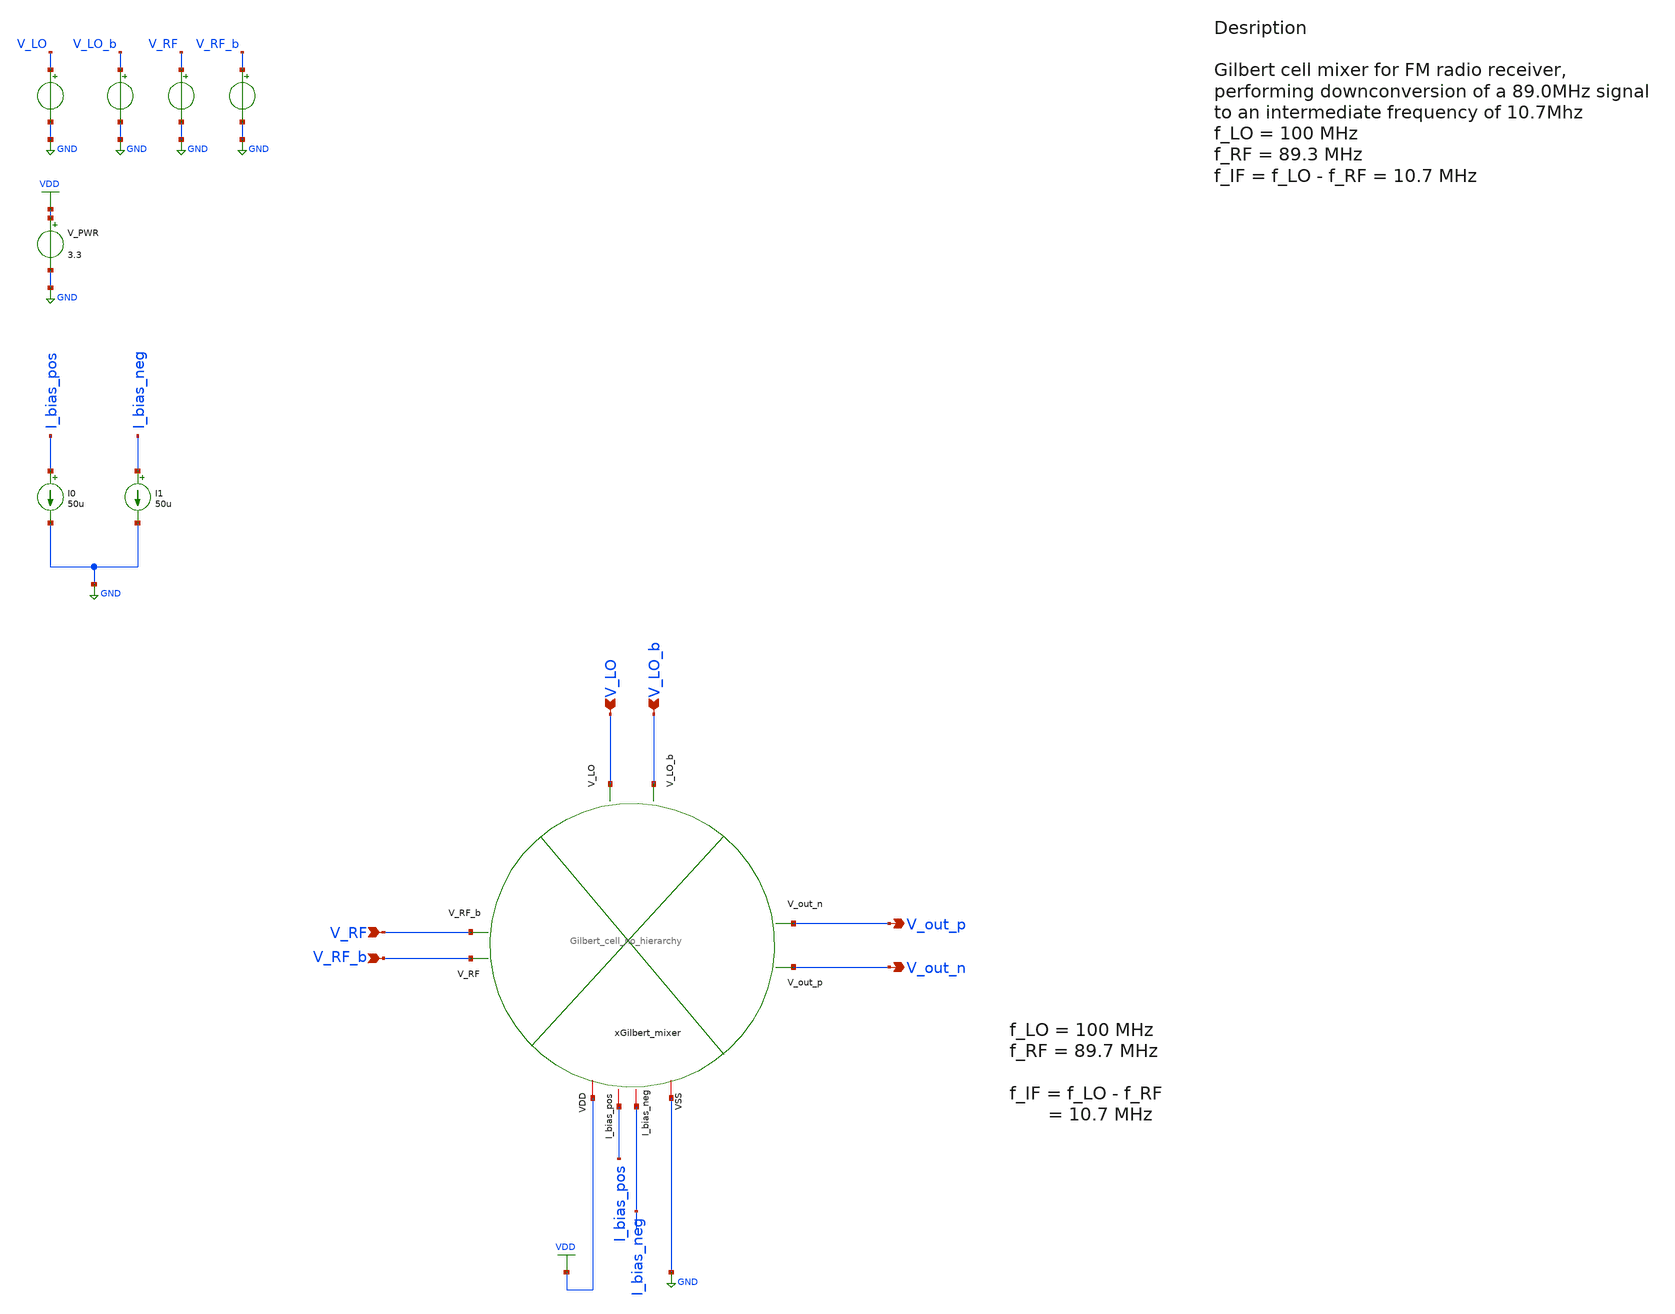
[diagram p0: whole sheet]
** sch_path: src/design_tb/Gilbert_cell_tb.sch
**.subckt Gilbert_cell_tb V_LO V_LO_b V_RF V_RF_b V_out_p V_out_n
*.ipin V_LO
*.ipin V_LO_b
*.ipin V_RF
*.ipin V_RF_b
*.opin V_out_p
*.opin V_out_n
V_PWR VDD GND 3.3
.save i(v_pwr)
V_LO V_LO GND pulse(0 1.5 0 1p 1p 0.25n 0.5n)
.save i(v_lo)
V_LO_b V_LO_b GND pulse(0 1.5 0 1p 1p 0.25n 0.5n)
.save i(v_lo_b)
V_RF V_RF GND sin( 1 1 1 0 )
.save i(v_rf)
V_RF_b V_RF_b GND sin( 1 1 1 0 0 180 )
.save i(v_rf_b)
xGilbert_mixer VDD V_out_n V_out_p V_LO V_LO_b V_RF_b V_RF I_bias_pos I_bias_neg GND
+ Gilbert_cell_no_hierarchy
I0 I_bias_pos GND 50u
I1 I_bias_neg GND 50u
**** begin user architecture code

.include $::180MCU_MODELS/design.ngspice
.lib $::180MCU_MODELS/sm141064.ngspice typical
.lib $::180MCU_MODELS/sm141064.ngspice mimcap_typical
.lib $::180MCU_MODELS/sm141064.ngspice cap_mim
.lib $::180MCU_MODELS/sm141064.ngspice res_typical




* let sets vectors to a plot, while set sets a variable, globally accessible in .control
.control

    * Set frequency and amplitude variables to proper values from within the control sequence
    * sine-wave LO
    * set cm_lo = 0.5
    * set freq_lo = 2.50G
    * set amp_lo = 0.5
    * alter @V_LO[sin] = [ $cm_lo $amp_lo $freq_lo 0 ]
    * alter @V_LO_b[sin] = [ $cm_lo $amp_lo $freq_lo 0 0 180 ]

    set freq_lo = 100Meg
    set cm_lo = 1.8
    set amp_lo = 0.4

    set cm_rf  = 1.2
    set freq_rf = 89.3Meg
    * set freq_rf = 10.7Meg
    set amp_rf  = 0.2

    * set the parameters to the voltage sources
    * alter @V_LO[pulse] = [ 2 2.5 0 0.5p 0.5p 5n 10n ]
    * alter @V_LO_b[pulse] = [ 2 2.5 5n 0.5p 0.5p 5n 10n]
    alter @V_LO[sin] = [ $cm_lo $amp_lo $freq_lo 0 ]
    alter @V_LO_b[sin] = [ $cm_lo $amp_lo $freq_lo 0 0 180 ]
    alter @V_RF[sin] = [ $cm_rf $amp_rf $freq_rf 0 ]
    alter @V_RF_b[sin] = [ $cm_rf $amp_rf $freq_rf 0 0 180 ]

    save all

    * operating point
    op
    show

    * save transistor op parameters
    * diff_pair_1 transistors
    save @m.xgilbert_mixer.xm_rf_pos.m0[vgs]
    save @m.xgilbert_mixer.xm_rf_pos.m0[vds]
    save @m.xgilbert_mixer.xm_rf_pos.m0[id]
    save @m.xgilbert_mixer.xm_rf_pos.m0[gm]
    save @m.xgilbert_mixer.xm_rf_pos.m0[vth]
    save @m.xgilbert_mixer.xm_rf_pos.m0[cgg]
    save @m.xgilbert_mixer.xm_rf_neg.m0[vgs]
    save @m.xgilbert_mixer.xm_rf_neg.m0[vds]
    save @m.xgilbert_mixer.xm_rf_neg.m0[id]
    save @m.xgilbert_mixer.xm_rf_neg.m0[gm]
    save @m.xgilbert_mixer.xm_rf_neg.m0[vth]
    save @m.xgilbert_mixer.xm_rf_neg.m0[cgg]

    * diff_pair_2 transistors
    * save @m.xdiff_pair_2.xm1.m0[vgs]
    * save @m.xdiff_pair_2.xm1.m0[vds]
    * save @m.xdiff_pair_2.xm1.m0[id]
    * save @m.xdiff_pair_2.xm1.m0[gm]
    * save @m.xdiff_pair_2.xm1.m0[vth]
    * save @m.xdiff_pair_2.xm1.m0[cgg]
    * save @m.xdiff_pair_2.xm2.m0[vgs]
    * save @m.xdiff_pair_2.xm2.m0[vds]
    * save @m.xdiff_pair_2.xm2.m0[id]
    * save @m.xdiff_pair_2.xm2.m0[gm]
    * save @m.xdiff_pair_2.xm2.m0[vth]
    * save @m.xdiff_pair_2.xm2.m0[cgg]

    * diff_pair_3 transistors
    * save @m.xdiff_pair_3.xm1.m0[vgs]
    * save @m.xdiff_pair_3.xm1.m0[vds]
    * save @m.xdiff_pair_3.xm1.m0[id]
    * save @m.xdiff_pair_3.xm1.m0[gm]
    * save @m.xdiff_pair_3.xm1.m0[vth]
    * save @m.xdiff_pair_3.xm1.m0[cgg]
    * save @m.xdiff_pair_3.xm2.m0[vgs]
    * save @m.xdiff_pair_3.xm2.m0[vds]
    * save @m.xdiff_pair_3.xm2.m0[id]
    * save @m.xdiff_pair_3.xm2.m0[gm]
    * save @m.xdiff_pair_3.xm2.m0[vth]
    * save @m.xdiff_pair_3.xm2.m0[cgg]

    write Gilbert_cell_tb_sim.raw

    set appendwrite

    * Transient analysis to observe mixing operation
    tran 1p 0.3u
    write Gilbert_cell_tb_sim.raw

    * Calculate differential output for conversion gain measurement
    let v_out_diff = v(v_out_p)-v(v_out_n)
    let v_rf_diff = v(v_rf)-v(v_rf_b)
    let v_lo_diff = v(v_lo)-v(v_lo_b)


    * Extract IF component at 100MHz using FFT
    linearize v_out_diff v_rf_diff v_lo_diff
    let time_step = 1e-12
    let sample_freq = 1/time_step
    let npts = length(v_out_diff)
    let freq_res = sample_freq/npts


    fft v_out_diff v_rf_diff v_lo_diff

    * print everything, sanity check
    * set     ; print all available global (?) variables (?)
    * setplot ; print all plots
    * display ; print variables available in current plot

    let freq_res = tran2.freq_res
    let freq_if = abs ( $freq_lo - $freq_rf )

    * Define bandwidth for power integration (10MHz around nominal frequencies).
    *  To improve resolution increase time of tran simulation, reduce time step, in order to reduce
+ FFT resolution
    let bandwidth = 10e6
    let bin_width = floor(bandwidth/freq_res + 0.5)

    * Find center bins for RF and IF frequencies
    let rf_center_bin = floor( $freq_rf/freq_res + 0.5 )
    let if_center_bin = floor( freq_if/freq_res + 0.5 )

    * Calculate power by summing magnitude squared over the bandwidth
    * RF power integration (±10MHz around freq_rf)
    let rf_power_total = 0
    let i = rf_center_bin - bin_width
    while i <= rf_center_bin + bin_width
        if i>0 & i < length(v_rf_diff)
            let bin_freq = i * freq_res
            * print bin_freq
            * print abs(v_rf_diff[i])
            let rf_power_total = rf_power_total + abs(v_rf_diff[i])^2
        end
        let i = i + 1
    end

    * IF power integration (±10MHz around freq_if)
    let if_power_total = 0
    let j = if_center_bin - bin_width
    while j <= if_center_bin + bin_width
        if j >= 0 & j < length(v_out_diff)
            let bin_freq = j * freq_res
            * print bin_freq
            * print abs(v_out_diff[j])
            let if_power_total = if_power_total + abs(v_out_diff[j])^2
        end
        let j = j + 1
    end

    print if_power_total
    print rf_power_total

    let conversion_gain_db = 10*log10(if_power_total/rf_power_total)
    print conversion_gain_db

    write Gilbert_cell_tb_sim.raw

.endc


**** end user architecture code
**.ends

* expanding   symbol:
*+  /home/vasil/Downloads/SSCS_PICO_2025/src/design_xsch/Gilbert_cell_no_hierarchy.sym # of pins=10
** sym_path: src/design_xsch/experimental_hierarchal/Gilbert_cell_no_hierarchy.sym
** sch_path: src/design_xsch/experimental_hierarchal/Gilbert_cell_no_hierarchy.sch
.subckt Gilbert_cell_no_hierarchy VDD V_out_p V_out_n V_LO V_LO_b V_RF V_RF_b I_bias_pos I_bias_neg
+ VSS
*.ipin V_LO
*.ipin V_LO_b
*.ipin V_RF
*.ipin V_RF_b
*.opin V_out_p
*.opin V_out_n
*.iopin I_bias_neg
*.iopin I_bias_pos
*.iopin VDD
*.iopin VSS
XM_dp_lo_pos V_out_p V_LO rf_diff_pair_pos_input VSS nfet_03v3 L=0.28u W=20u nf=5 ad='int((nf+1)/2) * W/nf * 0.18u'
+ as='int((nf+2)/2) * W/nf * 0.18u' pd='2*int((nf+1)/2) * (W/nf + 0.18u)' ps='2*int((nf+2)/2) * (W/nf + 0.18u)'
+ nrd='0.18u / W' nrs='0.18u / W' sa=0 sb=0 sd=0 m=1
XM_dp_lo_neg V_out_n V_LO_b rf_diff_pair_pos_input VSS nfet_03v3 L=0.28u W=20u nf=5 ad='int((nf+1)/2) * W/nf * 0.18u'
+ as='int((nf+2)/2) * W/nf * 0.18u' pd='2*int((nf+1)/2) * (W/nf + 0.18u)' ps='2*int((nf+2)/2) * (W/nf + 0.18u)'
+ nrd='0.18u / W' nrs='0.18u / W' sa=0 sb=0 sd=0 m=1
XM_dp_lo_b_pos V_out_p V_LO_b rf_diff_pair_neg_input VSS nfet_03v3 L=0.28u W=20u nf=5 ad='int((nf+1)/2) * W/nf * 0.18u'
+ as='int((nf+2)/2) * W/nf * 0.18u' pd='2*int((nf+1)/2) * (W/nf + 0.18u)' ps='2*int((nf+2)/2) * (W/nf + 0.18u)'
+ nrd='0.18u / W' nrs='0.18u / W' sa=0 sb=0 sd=0 m=1
XM_dp_lo_b_neg V_out_n V_LO rf_diff_pair_neg_input VSS nfet_03v3 L=0.28u W=20u nf=5 ad='int((nf+1)/2) * W/nf * 0.18u'
+ as='int((nf+2)/2) * W/nf * 0.18u' pd='2*int((nf+1)/2) * (W/nf + 0.18u)' ps='2*int((nf+2)/2) * (W/nf + 0.18u)'
+ nrd='0.18u / W' nrs='0.18u / W' sa=0 sb=0 sd=0 m=1
XM_rf_pos rf_diff_pair_pos_input V_RF I_bias_pos VSS nfet_03v3 L=0.28u W=10u nf=5 ad='int((nf+1)/2) * W/nf * 0.18u'
+ as='int((nf+2)/2) * W/nf * 0.18u' pd='2*int((nf+1)/2) * (W/nf + 0.18u)' ps='2*int((nf+2)/2) * (W/nf + 0.18u)'
+ nrd='0.18u / W' nrs='0.18u / W' sa=0 sb=0 sd=0 m=1
XM_rf_neg rf_diff_pair_neg_input V_RF_b I_bias_neg VSS nfet_03v3 L=0.28u W=10u nf=5 ad='int((nf+1)/2) * W/nf * 0.18u'
+ as='int((nf+2)/2) * W/nf * 0.18u' pd='2*int((nf+1)/2) * (W/nf + 0.18u)' ps='2*int((nf+2)/2) * (W/nf + 0.18u)'
+ nrd='0.18u / W' nrs='0.18u / W' sa=0 sb=0 sd=0 m=1
XR_load_3 I_bias_neg I_bias_pos VDD pplus_u r_width=0.5e-6 r_length=5e-6 m=1
XR_load_2 V_out_p VDD VDD ppolyf_u_1k r_width=1e-6 r_length=20e-6 m=1
XR_load_1 V_out_n VDD VDD ppolyf_u_1k r_width=1e-6 r_length=20e-6 m=1
.ends

.GLOBAL VDD
.GLOBAL GND
.end
